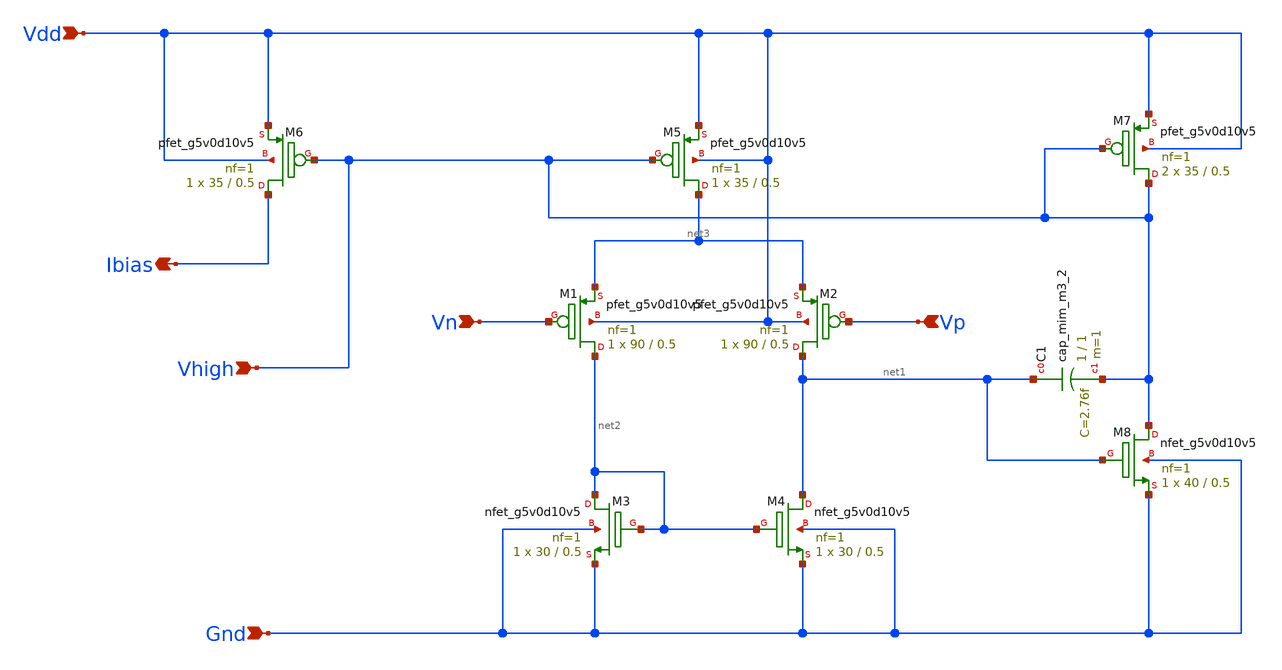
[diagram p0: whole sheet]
** sch_path: Analog_Blocks/LDO/Schematic/LDO_Folded_1.8v/Bandgap1.8v_OTA.sch
**.subckt Bandgap1.8v_OTA Ibias Vhigh Vdd Gnd Vp Vn
*.opin Ibias
*.ipin Vhigh
*.ipin Vdd
*.ipin Gnd
*.ipin Vp
*.ipin Vn
XM6 Ibias Vhigh Vdd Vdd sky130_fd_pr__pfet_g5v0d10v5 L=0.5 W=35 nf=1 ad='int((nf+1)/2) * W/nf * 0.29'
+ as='int((nf+2)/2) * W/nf * 0.29' pd='2*int((nf+1)/2) * (W/nf + 0.29)' ps='2*int((nf+2)/2) * (W/nf + 0.29)'
+ nrd='0.29 / W' nrs='0.29 / W' sa=0 sb=0 sd=0 mult=1 m=1
XM5 net3 Vhigh Vdd Vdd sky130_fd_pr__pfet_g5v0d10v5 L=0.5 W=35 nf=1 ad='int((nf+1)/2) * W/nf * 0.29'
+ as='int((nf+2)/2) * W/nf * 0.29' pd='2*int((nf+1)/2) * (W/nf + 0.29)' ps='2*int((nf+2)/2) * (W/nf + 0.29)'
+ nrd='0.29 / W' nrs='0.29 / W' sa=0 sb=0 sd=0 mult=1 m=1
XM1 net2 Vn net3 Vdd sky130_fd_pr__pfet_g5v0d10v5 L=0.5 W=90 nf=1 ad='int((nf+1)/2) * W/nf * 0.29' as='int((nf+2)/2) * W/nf * 0.29'
+ pd='2*int((nf+1)/2) * (W/nf + 0.29)' ps='2*int((nf+2)/2) * (W/nf + 0.29)' nrd='0.29 / W' nrs='0.29 / W'
+ sa=0 sb=0 sd=0 mult=1 m=1
XM8 Vhigh net1 Gnd Gnd sky130_fd_pr__nfet_g5v0d10v5 L=0.5 W=40 nf=1 ad='int((nf+1)/2) * W/nf * 0.29'
+ as='int((nf+2)/2) * W/nf * 0.29' pd='2*int((nf+1)/2) * (W/nf + 0.29)' ps='2*int((nf+2)/2) * (W/nf + 0.29)'
+ nrd='0.29 / W' nrs='0.29 / W' sa=0 sb=0 sd=0 mult=1 m=1
XM4 net1 net2 Gnd Gnd sky130_fd_pr__nfet_g5v0d10v5 L=0.5 W=30 nf=1 ad='int((nf+1)/2) * W/nf * 0.29' as='int((nf+2)/2) * W/nf * 0.29'
+ pd='2*int((nf+1)/2) * (W/nf + 0.29)' ps='2*int((nf+2)/2) * (W/nf + 0.29)' nrd='0.29 / W' nrs='0.29 / W'
+ sa=0 sb=0 sd=0 mult=1 m=1
XM3 net2 net2 Gnd Gnd sky130_fd_pr__nfet_g5v0d10v5 L=0.5 W=30 nf=1 ad='int((nf+1)/2) * W/nf * 0.29' as='int((nf+2)/2) * W/nf * 0.29'
+ pd='2*int((nf+1)/2) * (W/nf + 0.29)' ps='2*int((nf+2)/2) * (W/nf + 0.29)' nrd='0.29 / W' nrs='0.29 / W'
+ sa=0 sb=0 sd=0 mult=1 m=1
XC1 net1 Vhigh sky130_fd_pr__cap_mim_m3_2 W=1 L=1 MF=1 m=1
XM2 net1 Vp net3 Vdd sky130_fd_pr__pfet_g5v0d10v5 L=0.5 W=90 nf=1 ad='int((nf+1)/2) * W/nf * 0.29' as='int((nf+2)/2) * W/nf * 0.29'
+ pd='2*int((nf+1)/2) * (W/nf + 0.29)' ps='2*int((nf+2)/2) * (W/nf + 0.29)' nrd='0.29 / W' nrs='0.29 / W'
+ sa=0 sb=0 sd=0 mult=1 m=1
XM7 Vhigh Vhigh Vdd Vdd sky130_fd_pr__pfet_g5v0d10v5 L=0.5 W=35 nf=1 ad='int((nf+1)/2) * W/nf * 0.29'
+ as='int((nf+2)/2) * W/nf * 0.29' pd='2*int((nf+1)/2) * (W/nf + 0.29)' ps='2*int((nf+2)/2) * (W/nf + 0.29)'
+ nrd='0.29 / W' nrs='0.29 / W' sa=0 sb=0 sd=0 mult=2 m=2
**.ends
.end
